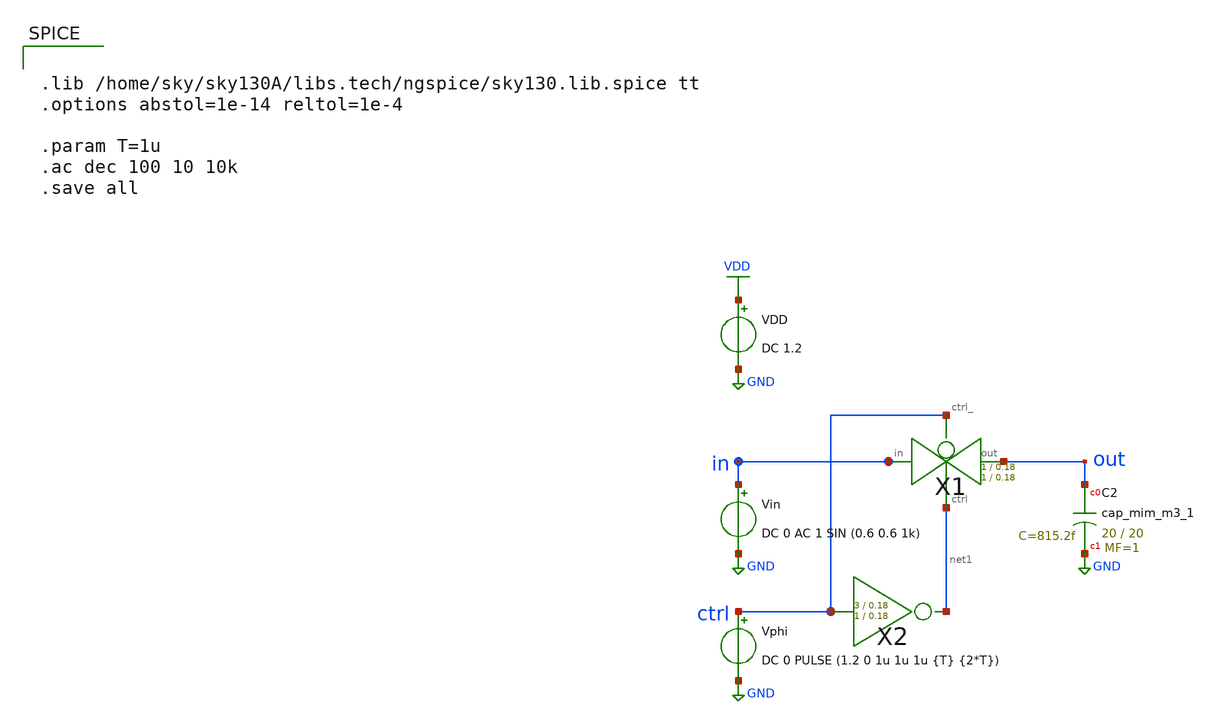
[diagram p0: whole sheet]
** sch_path: xschem/Switched_Caps/Characterizer_transmission_gate_plot.sch
**.subckt Characterizer_transmission_gate_plot
Vphi ctrl GND DC 0 PULSE (1.2 0 1u 1u 1u {T} {2*T})
XC2 out GND sky130_fd_pr__cap_mim_m3_1 W=20 L=20 MF=1 m=1
Vin in GND DC 0 AC 1 SIN (0.6 0.6 1k)
X1 in out ctrl net1 transmission_gate Wpmos=1 Lpmos=0.18 Wnmos=1 Lnmos=0.18
X2 ctrl net1 inv Wpmos=3 Lpmos=0.18 Wnmos=1 Lnmos=0.18
VDD VDD GND DC 1.2
**** begin user architecture code


.lib /home/sky/sky130A/libs.tech/ngspice/sky130.lib.spice tt
.options abstol=1e-14 reltol=1e-4

.param T=1u
.ac dec 100 10 10k
.save all


**** end user architecture code
**.ends

* expanding   symbol:  transmission_gate/transmission_gate.sym # of pins=4
** sym_path: xschem/transmission_gate/transmission_gate.sym
** sch_path: xschem/transmission_gate/transmission_gate.sch
.subckt transmission_gate in out ctrl_ ctrl  Wpmos=1 Lpmos=0.18 Wnmos=1 Lnmos=0.18
*.iopin in
*.iopin out
*.ipin ctrl_
*.ipin ctrl
XM1 in ctrl out GND sky130_fd_pr__nfet_01v8 L=Lnmos W=Wnmos nf=1 ad='int((nf+1)/2) * W/nf * 0.29' as='int((nf+2)/2) * W/nf * 0.29'
+ pd='2*int((nf+1)/2) * (W/nf + 0.29)' ps='2*int((nf+2)/2) * (W/nf + 0.29)' nrd='0.29 / W' nrs='0.29 / W'
+ sa=0 sb=0 sd=0 mult=1 m=1
XM2 out ctrl_ in VDD sky130_fd_pr__pfet_01v8 L=Lpmos W=Wpmos nf=1 ad='int((nf+1)/2) * W/nf * 0.29' as='int((nf+2)/2) * W/nf * 0.29'
+ pd='2*int((nf+1)/2) * (W/nf + 0.29)' ps='2*int((nf+2)/2) * (W/nf + 0.29)' nrd='0.29 / W' nrs='0.29 / W'
+ sa=0 sb=0 sd=0 mult=1 m=1
.ends


* expanding   symbol:  inv/inv.sym # of pins=2
** sym_path: xschem/inv/inv.sym
** sch_path: xschem/inv/inv.sch
.subckt inv in out  Wpmos=3 Lpmos=0.18 Wnmos=1 Lnmos=0.18
*.ipin in
*.iopin out
XM1 out in GND GND sky130_fd_pr__nfet_01v8 L=Lnmos W=Wnmos nf=1 ad='int((nf+1)/2) * W/nf * 0.29' as='int((nf+2)/2) * W/nf * 0.29'
+ pd='2*int((nf+1)/2) * (W/nf + 0.29)' ps='2*int((nf+2)/2) * (W/nf + 0.29)' nrd='0.29 / W' nrs='0.29 / W'
+ sa=0 sb=0 sd=0 mult=1 m=1
XM2 out in VDD VDD sky130_fd_pr__pfet_01v8 L=Lpmos W=Wpmos nf=1 ad='int((nf+1)/2) * W/nf * 0.29' as='int((nf+2)/2) * W/nf * 0.29'
+ pd='2*int((nf+1)/2) * (W/nf + 0.29)' ps='2*int((nf+2)/2) * (W/nf + 0.29)' nrd='0.29 / W' nrs='0.29 / W'
+ sa=0 sb=0 sd=0 mult=1 m=1
.ends

.GLOBAL GND
.GLOBAL VDD
.end
